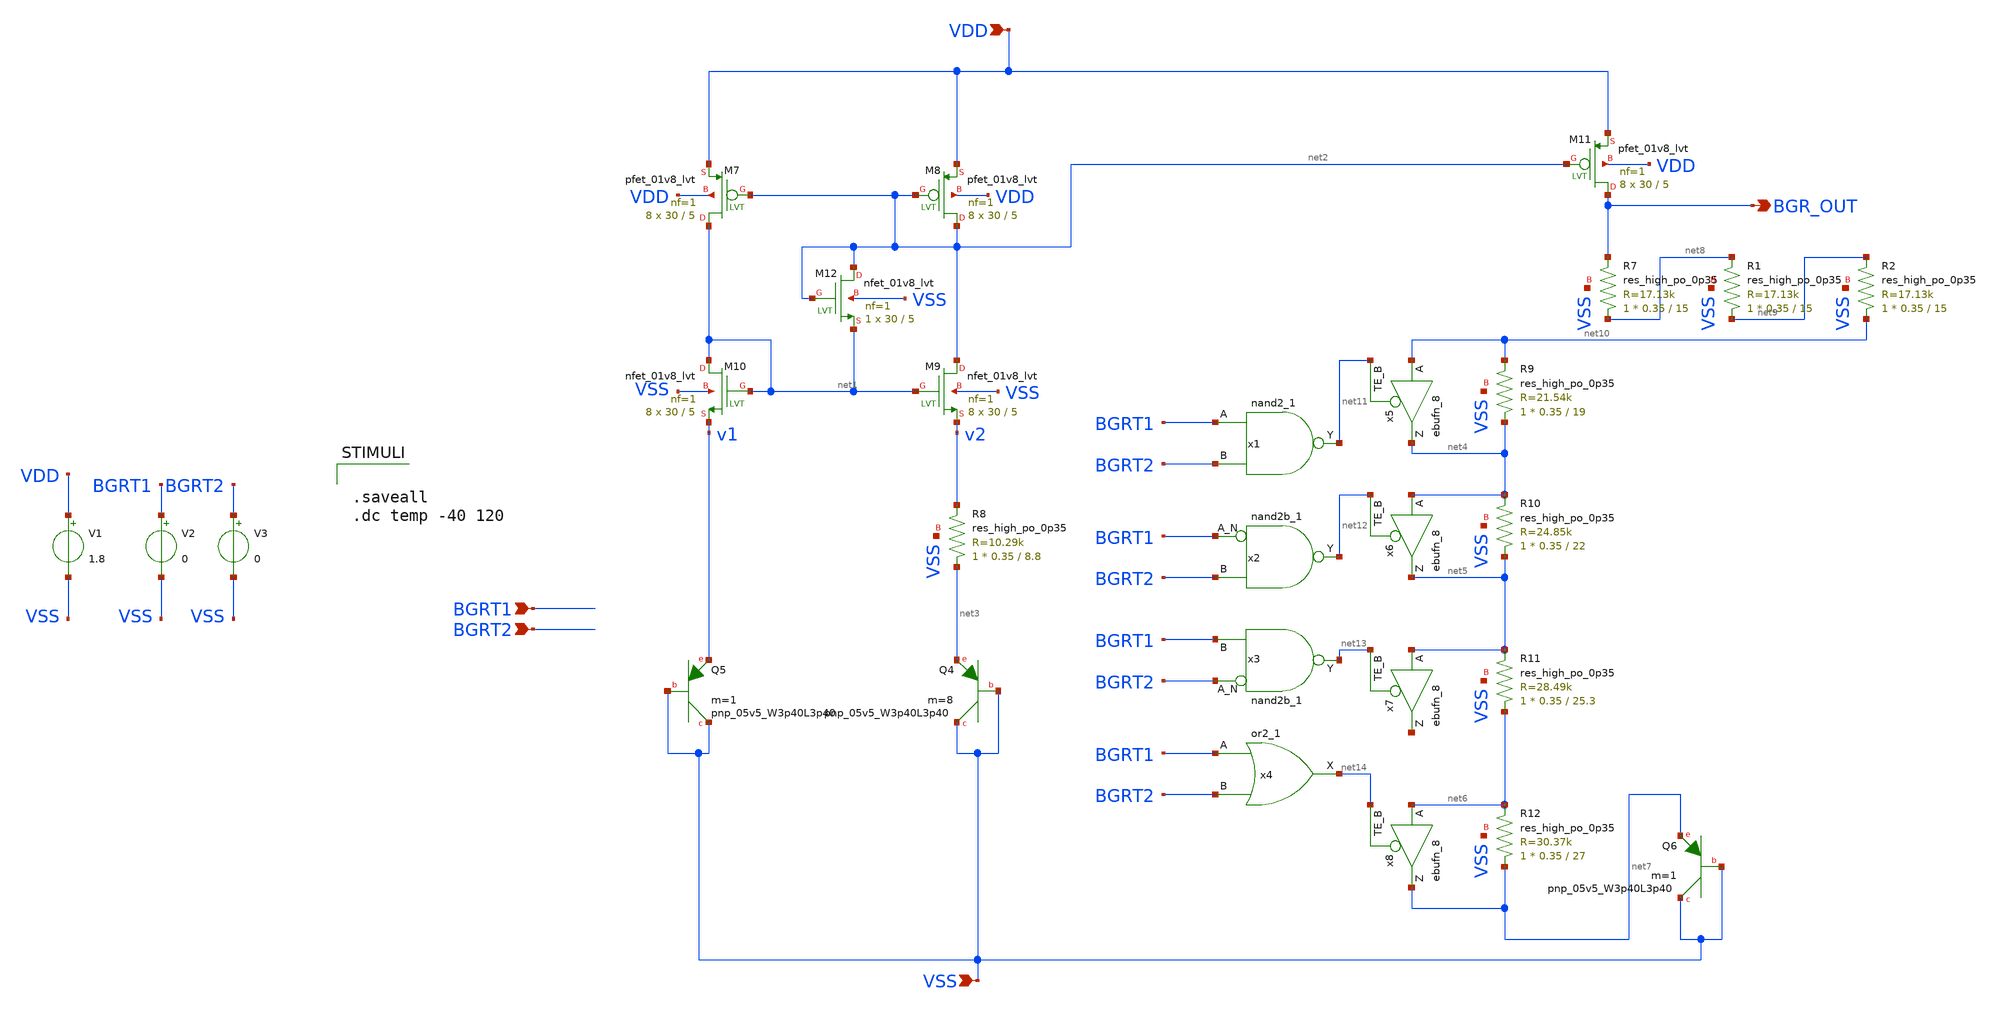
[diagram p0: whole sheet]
** sch_path: xschem/bandgap.sch
**.subckt bandgap BGR_OUT VDD VSS BGRT1 BGRT2
*.opin BGR_OUT
*.ipin VDD
*.ipin VSS
*.ipin BGRT1
*.ipin BGRT2
XM7 net1 net2 VDD VDD sky130_fd_pr__pfet_01v8_lvt L=5 W=30 nf=1 ad='int((nf+1)/2) * W/nf * 0.29' as='int((nf+2)/2) * W/nf * 0.29'
+ pd='2*int((nf+1)/2) * (W/nf + 0.29)' ps='2*int((nf+2)/2) * (W/nf + 0.29)' nrd='0.29 / W' nrs='0.29 / W'
+ sa=0 sb=0 sd=0 mult=8 m=8
XM8 net2 net2 VDD VDD sky130_fd_pr__pfet_01v8_lvt L=5 W=30 nf=1 ad='int((nf+1)/2) * W/nf * 0.29' as='int((nf+2)/2) * W/nf * 0.29'
+ pd='2*int((nf+1)/2) * (W/nf + 0.29)' ps='2*int((nf+2)/2) * (W/nf + 0.29)' nrd='0.29 / W' nrs='0.29 / W'
+ sa=0 sb=0 sd=0 mult=8 m=8
XM9 net2 net1 v2 VSS sky130_fd_pr__nfet_01v8_lvt L=5 W=30 nf=1 ad='int((nf+1)/2) * W/nf * 0.29' as='int((nf+2)/2) * W/nf * 0.29'
+ pd='2*int((nf+1)/2) * (W/nf + 0.29)' ps='2*int((nf+2)/2) * (W/nf + 0.29)' nrd='0.29 / W' nrs='0.29 / W'
+ sa=0 sb=0 sd=0 mult=8 m=8
XM10 net1 net1 v1 VSS sky130_fd_pr__nfet_01v8_lvt L=5 W=30 nf=1 ad='int((nf+1)/2) * W/nf * 0.29' as='int((nf+2)/2) * W/nf * 0.29'
+ pd='2*int((nf+1)/2) * (W/nf + 0.29)' ps='2*int((nf+2)/2) * (W/nf + 0.29)' nrd='0.29 / W' nrs='0.29 / W'
+ sa=0 sb=0 sd=0 mult=8 m=8
XQ4 VSS VSS net3 sky130_fd_pr__pnp_05v5_W3p40L3p40 m=8
XQ5 VSS VSS v1 sky130_fd_pr__pnp_05v5_W3p40L3p40 m=1
XM11 BGR_OUT net2 VDD VDD sky130_fd_pr__pfet_01v8_lvt L=5 W=30 nf=1 ad='int((nf+1)/2) * W/nf * 0.29'
+ as='int((nf+2)/2) * W/nf * 0.29' pd='2*int((nf+1)/2) * (W/nf + 0.29)' ps='2*int((nf+2)/2) * (W/nf + 0.29)'
+ nrd='0.29 / W' nrs='0.29 / W' sa=0 sb=0 sd=0 mult=8 m=8
XR7 net8 BGR_OUT VSS sky130_fd_pr__res_high_po_0p35 L=15 mult=1 m=1
XM12 net2 net2 net1 VSS sky130_fd_pr__nfet_01v8_lvt L=5 W=30 nf=1 ad='int((nf+1)/2) * W/nf * 0.29' as='int((nf+2)/2) * W/nf * 0.29'
+ pd='2*int((nf+1)/2) * (W/nf + 0.29)' ps='2*int((nf+2)/2) * (W/nf + 0.29)' nrd='0.29 / W' nrs='0.29 / W'
+ sa=0 sb=0 sd=0 mult=1 m=1
XR8 net3 v2 VSS sky130_fd_pr__res_high_po_0p35 L=8.8 mult=1 m=1
XR9 net4 net10 VSS sky130_fd_pr__res_high_po_0p35 L=19 mult=1 m=1
XR10 net5 net4 VSS sky130_fd_pr__res_high_po_0p35 L=22 mult=1 m=1
XR11 net6 net5 VSS sky130_fd_pr__res_high_po_0p35 L=25.3 mult=1 m=1
XR12 net7 net6 VSS sky130_fd_pr__res_high_po_0p35 L=27 mult=1 m=1
XQ6 VSS VSS net7 sky130_fd_pr__pnp_05v5_W3p40L3p40 m=1
XR1 net9 net8 VSS sky130_fd_pr__res_high_po_0p35 L=15 mult=1 m=1
XR2 net10 net9 VSS sky130_fd_pr__res_high_po_0p35 L=15 mult=1 m=1
x1 BGRT1 BGRT2 VGND VNB VPB VPWR net11 sky130_fd_sc_hd__nand2_1
x2 BGRT1 BGRT2 VGND VNB VPB VPWR net12 sky130_fd_sc_hd__nand2b_1
x3 BGRT2 BGRT1 VGND VNB VPB VPWR net13 sky130_fd_sc_hd__nand2b_1
x4 BGRT1 BGRT2 VGND VNB VPB VPWR net14 sky130_fd_sc_hd__or2_1
x5 net10 net11 VGND VNB VPB VPWR net4 sky130_fd_sc_hd__ebufn_8
x6 net4 net12 VGND VNB VPB VPWR net5 sky130_fd_sc_hd__ebufn_8
x7 net5 net13 VGND VNB VPB VPWR net15 sky130_fd_sc_hd__ebufn_8
x8 net6 net14 VGND VNB VPB VPWR net7 sky130_fd_sc_hd__ebufn_8
V1 VDD VSS 1.8
V2 BGRT1 VSS 0
V3 BGRT2 VSS 0
**** begin user architecture code


.saveall
.dc temp -40 120



.param mc_mm_switch=0
.param mc_pr_switch=0
.include ~/mabrains/Analog_blocks/models/sky130A/libs.ref/sky130_fd_pr/spice/sky130_fd_pr__nfet_01v8__tt.corner.spice
.include ~/mabrains/Analog_blocks/models/sky130A/libs.ref/sky130_fd_pr/spice/sky130_fd_pr__nfet_01v8_lvt__tt.corner.spice
.include ~/mabrains/Analog_blocks/models/sky130A/libs.ref/sky130_fd_pr/spice/sky130_fd_pr__pfet_01v8__tt.corner.spice
.include ~/mabrains/Analog_blocks/models/sky130A/libs.ref/sky130_fd_pr/spice/sky130_fd_pr__nfet_03v3_nvt__tt.corner.spice
.include ~/mabrains/Analog_blocks/models/sky130A/libs.ref/sky130_fd_pr/spice/sky130_fd_pr__nfet_05v0_nvt__tt.corner.spice
.include ~/mabrains/Analog_blocks/models/sky130A/libs.ref/sky130_fd_pr/spice/sky130_fd_pr__esd_nfet_01v8__tt.corner.spice
.include ~/mabrains/Analog_blocks/models/sky130A/libs.ref/sky130_fd_pr/spice/sky130_fd_pr__pfet_01v8_lvt__tt.corner.spice
.include ~/mabrains/Analog_blocks/models/sky130A/libs.ref/sky130_fd_pr/spice/sky130_fd_pr__pfet_01v8_hvt__tt.corner.spice
.include ~/mabrains/Analog_blocks/models/sky130A/libs.ref/sky130_fd_pr/spice/sky130_fd_pr__esd_pfet_g5v0d10v5__tt.corner.spice
.include ~/mabrains/Analog_blocks/models/sky130A/libs.ref/sky130_fd_pr/spice/sky130_fd_pr__pfet_g5v0d10v5__tt.corner.spice
.include ~/mabrains/Analog_blocks/models/sky130A/libs.ref/sky130_fd_pr/spice/sky130_fd_pr__pfet_g5v0d16v0__tt.corner.spice
.include ~/mabrains/Analog_blocks/models/sky130A/libs.ref/sky130_fd_pr/spice/sky130_fd_pr__nfet_g5v0d10v5__tt.corner.spice
.include ~/mabrains/Analog_blocks/models/sky130A/libs.ref/sky130_fd_pr/spice/sky130_fd_pr__nfet_g5v0d16v0__tt_discrete.corner.spice
.include ~/mabrains/Analog_blocks/models/sky130A/libs.ref/sky130_fd_pr/spice/sky130_fd_pr__esd_nfet_g5v0d10v5__tt.corner.spice
.include ~/mabrains/Analog_blocks/models/sky130A/libs.tech/ngspice/corners/tt/nonfet.spice
* Mismatch parameters
.include ~/mabrains/Analog_blocks/models/sky130A/libs.ref/sky130_fd_pr/spice/sky130_fd_pr__nfet_01v8__mismatch.corner.spice
.include ~/mabrains/Analog_blocks/models/sky130A/libs.ref/sky130_fd_pr/spice/sky130_fd_pr__pfet_01v8__mismatch.corner.spice
.include ~/mabrains/Analog_blocks/models/sky130A/libs.ref/sky130_fd_pr/spice/sky130_fd_pr__nfet_01v8_lvt__mismatch.corner.spice
.include ~/mabrains/Analog_blocks/models/sky130A/libs.ref/sky130_fd_pr/spice/sky130_fd_pr__pfet_01v8_lvt__mismatch.corner.spice
.include ~/mabrains/Analog_blocks/models/sky130A/libs.ref/sky130_fd_pr/spice/sky130_fd_pr__pfet_01v8_hvt__mismatch.corner.spice
.include ~/mabrains/Analog_blocks/models/sky130A/libs.ref/sky130_fd_pr/spice/sky130_fd_pr__nfet_g5v0d10v5__mismatch.corner.spice
.include ~/mabrains/Analog_blocks/models/sky130A/libs.ref/sky130_fd_pr/spice/sky130_fd_pr__pfet_g5v0d10v5__mismatch.corner.spice
.include ~/mabrains/Analog_blocks/models/sky130A/libs.ref/sky130_fd_pr/spice/sky130_fd_pr__nfet_05v0_nvt__mismatch.corner.spice
.include ~/mabrains/Analog_blocks/models/sky130A/libs.ref/sky130_fd_pr/spice/sky130_fd_pr__nfet_03v3_nvt__mismatch.corner.spice
* Resistor/Capacitor
.include ~/mabrains/Analog_blocks/models/sky130A/libs.tech/ngspice/r+c/res_typical__cap_typical.spice
.include ~/mabrains/Analog_blocks/models/sky130A/libs.tech/ngspice/r+c/res_typical__cap_typical__lin.spice
* Special cells
.include ~/mabrains/Analog_blocks/models/sky130A/libs.tech/ngspice/corners/tt/specialized_cells.spice
* All models
.include ~/mabrains/Analog_blocks/models/sky130A/libs.tech/ngspice/all.spice
* Corner
.include ~/mabrains/Analog_blocks/models/sky130A/libs.tech/ngspice/corners/tt/rf.spice



**** end user architecture code
**.ends
.end
